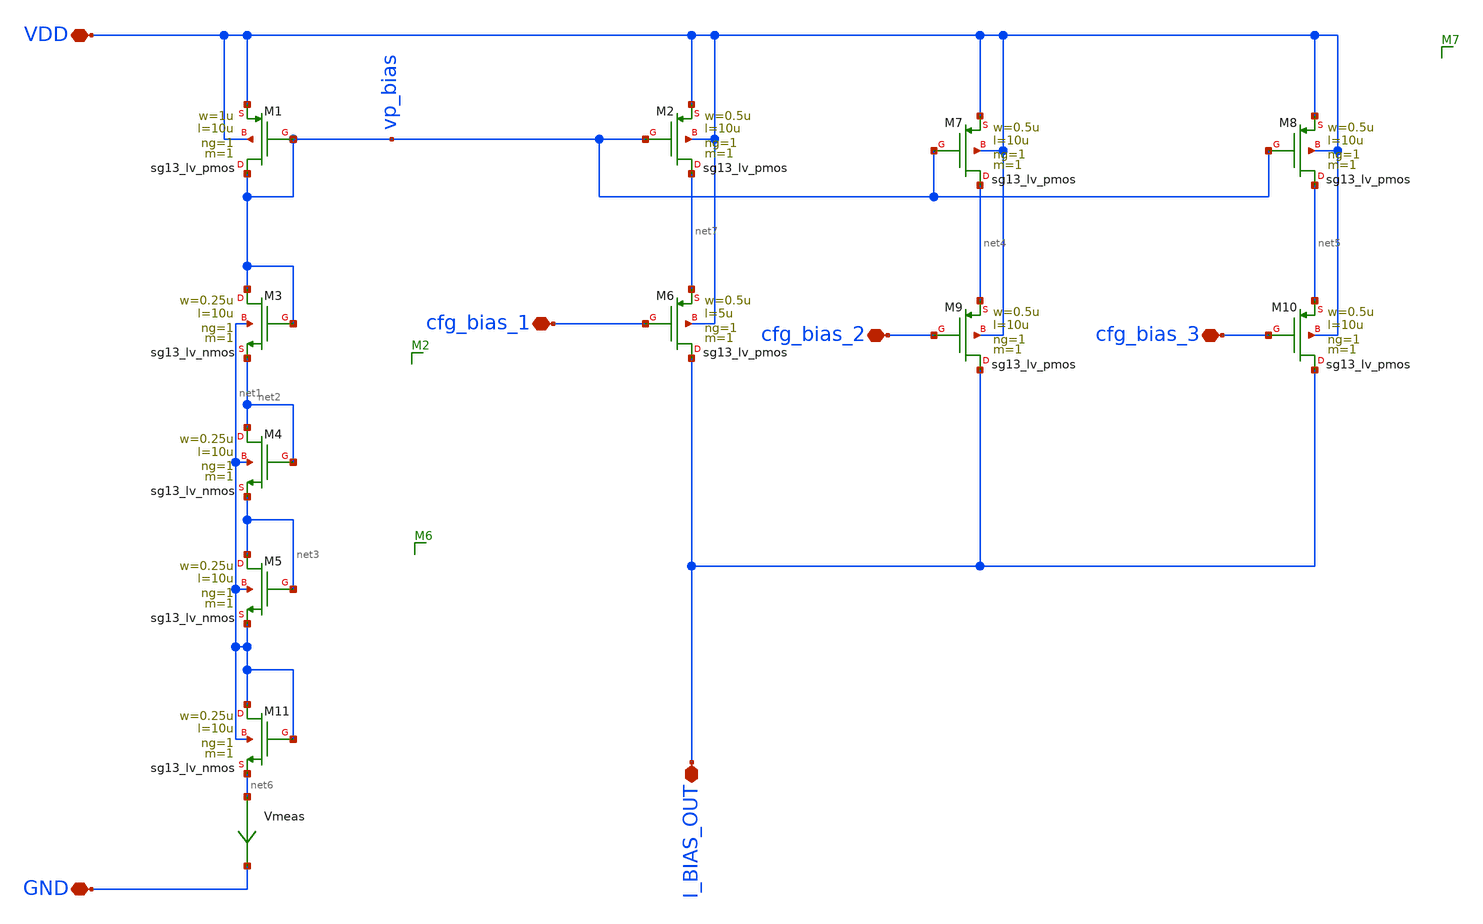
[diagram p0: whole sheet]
** sch_path: osc_bias.sch
**.subckt osc_bias VDD GND I_BIAS_OUT cfg_bias_1 cfg_bias_2 cfg_bias_3
*.iopin VDD
*.iopin GND
*.iopin I_BIAS_OUT
*.iopin cfg_bias_1
*.iopin cfg_bias_2
*.iopin cfg_bias_3
XM1 vp_bias vp_bias VDD VDD sg13_lv_pmos w=1u l=10u ng=1 m=1 mm_ok=1
XM3 vp_bias vp_bias net2 net1 sg13_lv_nmos w=0.25u l=10u ng=1 m=1 mm_ok=1
XM4 net2 net2 net3 net1 sg13_lv_nmos w=0.25u l=10u ng=1 m=1 mm_ok=1
XM5 net3 net3 net1 net1 sg13_lv_nmos w=0.25u l=10u ng=1 m=1 mm_ok=1
XM2 net7 vp_bias VDD VDD sg13_lv_pmos w=0.5u l=10u ng=1 m=1 mm_ok=1
XM6 I_BIAS_OUT cfg_bias_1 net7 VDD sg13_lv_pmos w=0.5u l=5u ng=1 m=1 mm_ok=1
XM7 net4 vp_bias VDD VDD sg13_lv_pmos w=0.5u l=10u ng=1 m=1 mm_ok=1
XM8 net5 vp_bias VDD VDD sg13_lv_pmos w=0.5u l=10u ng=1 m=1 mm_ok=1
XM9 I_BIAS_OUT cfg_bias_2 net4 VDD sg13_lv_pmos w=0.5u l=10u ng=1 m=1 mm_ok=1
XM10 I_BIAS_OUT cfg_bias_3 net5 VDD sg13_lv_pmos w=0.5u l=10u ng=1 m=1 mm_ok=1
XM11 net1 net1 net6 net1 sg13_lv_nmos w=0.25u l=10u ng=1 m=1 mm_ok=1
Vmeas net6 GND 0
.save i(vmeas)
**.ends
.end
